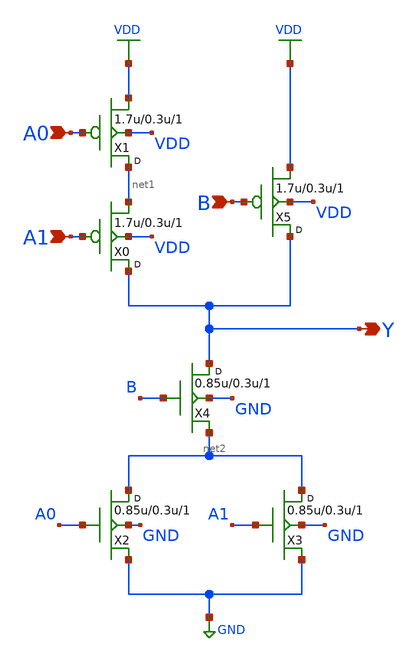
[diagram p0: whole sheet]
** sch_path: lib/9T/xschem/gf180mcu_osu_sc_oai21_1.sch
**.subckt gf180mcu_osu_sc_oai21_1 A0 A1 Y B
*.ipin A0
*.ipin A1
*.opin Y
*.ipin B
X1 net1 A0 VDD VDD pmos_3p3 w=1.7u l=0.3u m=1
X0 Y A1 net1 VDD pmos_3p3 w=1.7u l=0.3u m=1
X2 net2 A0 GND GND nmos_3p3 w=0.85u l=0.3u m=1
X3 net2 A1 GND GND nmos_3p3 w=0.85u l=0.3u m=1
X4 Y B net2 GND nmos_3p3 w=0.85u l=0.3u m=1
X5 Y B VDD VDD pmos_3p3 w=1.7u l=0.3u m=1
**** begin user architecture code


.inc "/import/yukari1/lrburle/OSU_180/char/techfiles/design.hspice"
.lib "/import/yukari1/lrburle/OSU_180/char/techfiles/sm141064.hspice" typical


**** end user architecture code
**.ends
.GLOBAL VDD
.GLOBAL GND
.end
